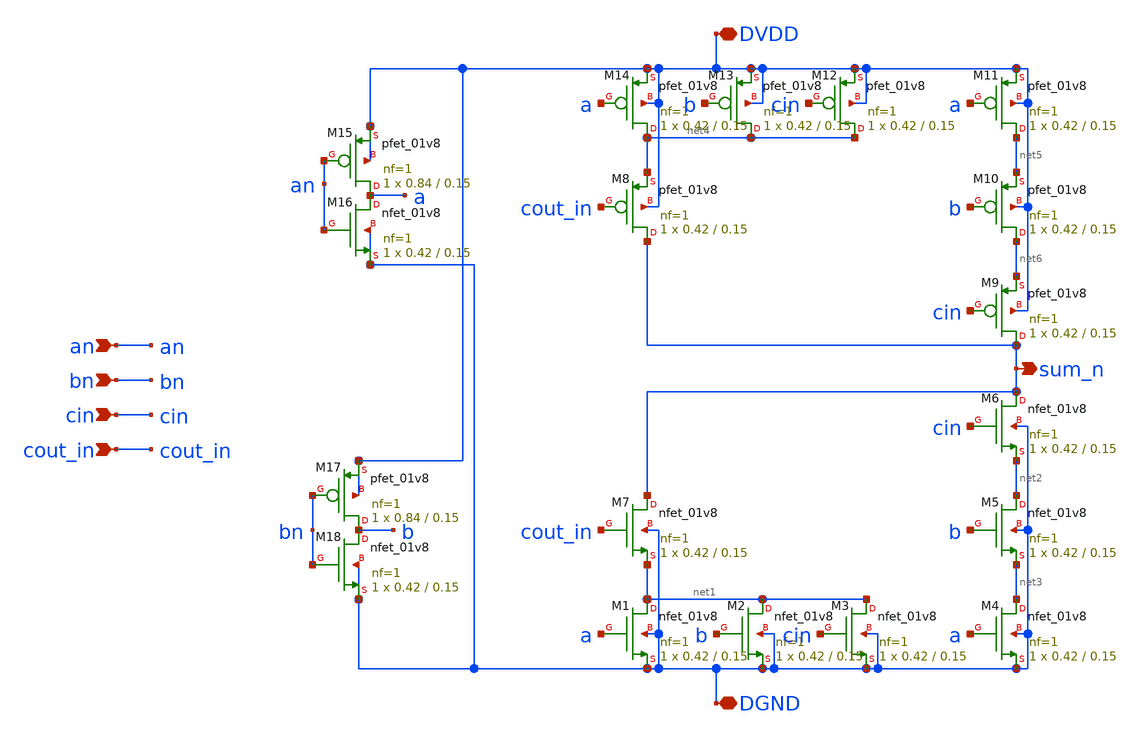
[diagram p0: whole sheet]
** sch_path: tut6/again/sim/sum.sch
**.subckt sum an bn cin DGND cout_in DVDD sum_n
*.ipin an
*.ipin bn
*.ipin cin
*.iopin DGND
*.ipin cout_in
*.iopin DVDD
*.opin sum_n
XM1 net1 a DGND DGND sky130_fd_pr__nfet_01v8 L=0.15 W=0.42 nf=1 ad='int((nf+1)/2) * W/nf * 0.29' as='int((nf+2)/2) * W/nf * 0.29'
+ pd='2*int((nf+1)/2) * (W/nf + 0.29)' ps='2*int((nf+2)/2) * (W/nf + 0.29)' nrd='0.29 / W' nrs='0.29 / W'
+ sa=0 sb=0 sd=0 mult=1 m=1
XM2 net1 b DGND DGND sky130_fd_pr__nfet_01v8 L=0.15 W=0.42 nf=1 ad='int((nf+1)/2) * W/nf * 0.29' as='int((nf+2)/2) * W/nf * 0.29'
+ pd='2*int((nf+1)/2) * (W/nf + 0.29)' ps='2*int((nf+2)/2) * (W/nf + 0.29)' nrd='0.29 / W' nrs='0.29 / W'
+ sa=0 sb=0 sd=0 mult=1 m=1
XM3 net1 cin DGND DGND sky130_fd_pr__nfet_01v8 L=0.15 W=0.42 nf=1 ad='int((nf+1)/2) * W/nf * 0.29' as='int((nf+2)/2) * W/nf * 0.29'
+ pd='2*int((nf+1)/2) * (W/nf + 0.29)' ps='2*int((nf+2)/2) * (W/nf + 0.29)' nrd='0.29 / W' nrs='0.29 / W'
+ sa=0 sb=0 sd=0 mult=1 m=1
XM4 net3 a DGND DGND sky130_fd_pr__nfet_01v8 L=0.15 W=0.42 nf=1 ad='int((nf+1)/2) * W/nf * 0.29' as='int((nf+2)/2) * W/nf * 0.29'
+ pd='2*int((nf+1)/2) * (W/nf + 0.29)' ps='2*int((nf+2)/2) * (W/nf + 0.29)' nrd='0.29 / W' nrs='0.29 / W'
+ sa=0 sb=0 sd=0 mult=1 m=1
XM5 net2 b net3 DGND sky130_fd_pr__nfet_01v8 L=0.15 W=0.42 nf=1 ad='int((nf+1)/2) * W/nf * 0.29' as='int((nf+2)/2) * W/nf * 0.29'
+ pd='2*int((nf+1)/2) * (W/nf + 0.29)' ps='2*int((nf+2)/2) * (W/nf + 0.29)' nrd='0.29 / W' nrs='0.29 / W'
+ sa=0 sb=0 sd=0 mult=1 m=1
XM6 sum_n cin net2 DGND sky130_fd_pr__nfet_01v8 L=0.15 W=0.42 nf=1 ad='int((nf+1)/2) * W/nf * 0.29' as='int((nf+2)/2) * W/nf * 0.29'
+ pd='2*int((nf+1)/2) * (W/nf + 0.29)' ps='2*int((nf+2)/2) * (W/nf + 0.29)' nrd='0.29 / W' nrs='0.29 / W'
+ sa=0 sb=0 sd=0 mult=1 m=1
XM7 sum_n cout_in net1 DGND sky130_fd_pr__nfet_01v8 L=0.15 W=0.42 nf=1 ad='int((nf+1)/2) * W/nf * 0.29'
+ as='int((nf+2)/2) * W/nf * 0.29' pd='2*int((nf+1)/2) * (W/nf + 0.29)' ps='2*int((nf+2)/2) * (W/nf + 0.29)'
+ nrd='0.29 / W' nrs='0.29 / W' sa=0 sb=0 sd=0 mult=1 m=1
XM8 sum_n cout_in net4 DVDD sky130_fd_pr__pfet_01v8 L=0.15 W=0.42 nf=1 ad='int((nf+1)/2) * W/nf * 0.29'
+ as='int((nf+2)/2) * W/nf * 0.29' pd='2*int((nf+1)/2) * (W/nf + 0.29)' ps='2*int((nf+2)/2) * (W/nf + 0.29)'
+ nrd='0.29 / W' nrs='0.29 / W' sa=0 sb=0 sd=0 mult=1 m=1
XM9 sum_n cin net6 DVDD sky130_fd_pr__pfet_01v8 L=0.15 W=0.42 nf=1 ad='int((nf+1)/2) * W/nf * 0.29' as='int((nf+2)/2) * W/nf * 0.29'
+ pd='2*int((nf+1)/2) * (W/nf + 0.29)' ps='2*int((nf+2)/2) * (W/nf + 0.29)' nrd='0.29 / W' nrs='0.29 / W'
+ sa=0 sb=0 sd=0 mult=1 m=1
XM10 net6 b net5 DVDD sky130_fd_pr__pfet_01v8 L=0.15 W=0.42 nf=1 ad='int((nf+1)/2) * W/nf * 0.29' as='int((nf+2)/2) * W/nf * 0.29'
+ pd='2*int((nf+1)/2) * (W/nf + 0.29)' ps='2*int((nf+2)/2) * (W/nf + 0.29)' nrd='0.29 / W' nrs='0.29 / W'
+ sa=0 sb=0 sd=0 mult=1 m=1
XM11 net5 a DVDD DVDD sky130_fd_pr__pfet_01v8 L=0.15 W=0.42 nf=1 ad='int((nf+1)/2) * W/nf * 0.29' as='int((nf+2)/2) * W/nf * 0.29'
+ pd='2*int((nf+1)/2) * (W/nf + 0.29)' ps='2*int((nf+2)/2) * (W/nf + 0.29)' nrd='0.29 / W' nrs='0.29 / W'
+ sa=0 sb=0 sd=0 mult=1 m=1
XM12 net4 cin DVDD DVDD sky130_fd_pr__pfet_01v8 L=0.15 W=0.42 nf=1 ad='int((nf+1)/2) * W/nf * 0.29' as='int((nf+2)/2) * W/nf * 0.29'
+ pd='2*int((nf+1)/2) * (W/nf + 0.29)' ps='2*int((nf+2)/2) * (W/nf + 0.29)' nrd='0.29 / W' nrs='0.29 / W'
+ sa=0 sb=0 sd=0 mult=1 m=1
XM13 net4 b DVDD DVDD sky130_fd_pr__pfet_01v8 L=0.15 W=0.42 nf=1 ad='int((nf+1)/2) * W/nf * 0.29' as='int((nf+2)/2) * W/nf * 0.29'
+ pd='2*int((nf+1)/2) * (W/nf + 0.29)' ps='2*int((nf+2)/2) * (W/nf + 0.29)' nrd='0.29 / W' nrs='0.29 / W'
+ sa=0 sb=0 sd=0 mult=1 m=1
XM14 net4 a DVDD DVDD sky130_fd_pr__pfet_01v8 L=0.15 W=0.42 nf=1 ad='int((nf+1)/2) * W/nf * 0.29' as='int((nf+2)/2) * W/nf * 0.29'
+ pd='2*int((nf+1)/2) * (W/nf + 0.29)' ps='2*int((nf+2)/2) * (W/nf + 0.29)' nrd='0.29 / W' nrs='0.29 / W'
+ sa=0 sb=0 sd=0 mult=1 m=1
XM15 a an DVDD DVDD sky130_fd_pr__pfet_01v8 L=0.15 W=0.84 nf=1 ad='int((nf+1)/2) * W/nf * 0.29' as='int((nf+2)/2) * W/nf * 0.29'
+ pd='2*int((nf+1)/2) * (W/nf + 0.29)' ps='2*int((nf+2)/2) * (W/nf + 0.29)' nrd='0.29 / W' nrs='0.29 / W'
+ sa=0 sb=0 sd=0 mult=1 m=1
XM16 a an DGND DGND sky130_fd_pr__nfet_01v8 L=0.15 W=0.42 nf=1 ad='int((nf+1)/2) * W/nf * 0.29' as='int((nf+2)/2) * W/nf * 0.29'
+ pd='2*int((nf+1)/2) * (W/nf + 0.29)' ps='2*int((nf+2)/2) * (W/nf + 0.29)' nrd='0.29 / W' nrs='0.29 / W'
+ sa=0 sb=0 sd=0 mult=1 m=1
XM17 b bn DVDD DVDD sky130_fd_pr__pfet_01v8 L=0.15 W=0.84 nf=1 ad='int((nf+1)/2) * W/nf * 0.29' as='int((nf+2)/2) * W/nf * 0.29'
+ pd='2*int((nf+1)/2) * (W/nf + 0.29)' ps='2*int((nf+2)/2) * (W/nf + 0.29)' nrd='0.29 / W' nrs='0.29 / W'
+ sa=0 sb=0 sd=0 mult=1 m=1
XM18 b bn DGND DGND sky130_fd_pr__nfet_01v8 L=0.15 W=0.42 nf=1 ad='int((nf+1)/2) * W/nf * 0.29' as='int((nf+2)/2) * W/nf * 0.29'
+ pd='2*int((nf+1)/2) * (W/nf + 0.29)' ps='2*int((nf+2)/2) * (W/nf + 0.29)' nrd='0.29 / W' nrs='0.29 / W'
+ sa=0 sb=0 sd=0 mult=1 m=1
**.ends
.end
